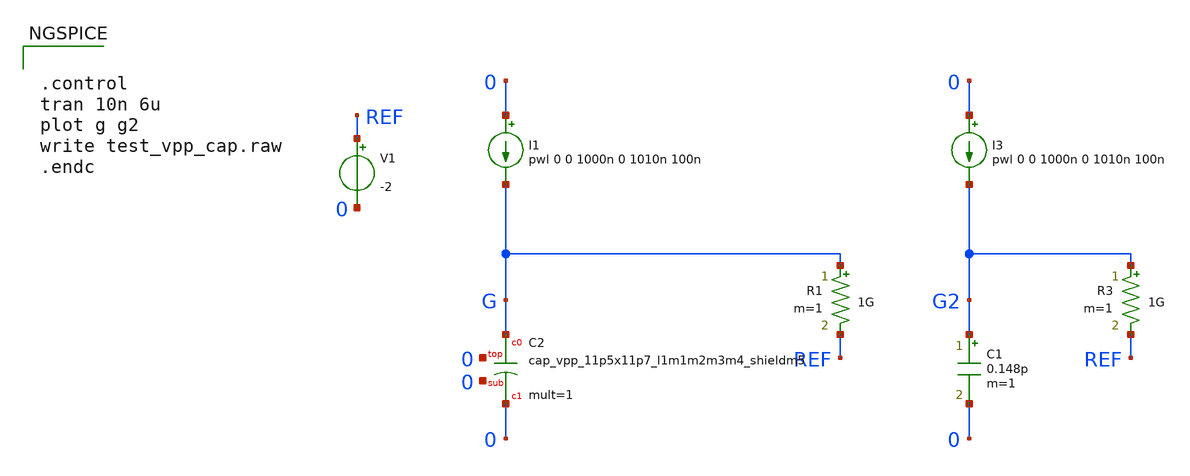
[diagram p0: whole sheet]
** sch_path: sky130_tests/test_vpp_cap.sch
* Copyright 2021 Stefan Frederik Schippers
* Licensed under the Apache License, Version 2.0 (the "License");
* you may not use this file except in compliance with the License.
* You may obtain a copy of the License at
* https://www.apache.org/licenses/LICENSE-2.0
* Unless required by applicable law or agreed to in writing, software
* distributed under the License is distributed on an "AS IS" BASIS,
* WITHOUT WARRANTIES OR CONDITIONS OF ANY KIND, either express or implied.
* See the License for the specific language governing permissions and
* limitations under the License.
**.subckt test_vpp_cap
I1 0 G pwl 0 0 1000n 0 1010n 100n
R1 G REF 1G m=1
I3 0 G2 pwl 0 0 1000n 0 1010n 100n
R3 G2 REF 1G m=1
C1 G2 0 0.148p m=1
V1 REF 0 -2
XC2 G 0 0 0 sky130_fd_pr__cap_vpp_11p5x11p7_l1m1m2m3m4_shieldm5 W=1 L=1 mult=1 m=1
**** begin user architecture code


.control
tran 10n 6u
plot g g2
write test_vpp_cap.raw
.endc


 ** manual skywater pdks install (with patches applied)
* .lib $::SKYWATER_MODELS/models/sky130.lib.spice tt

** opencircuitdesign pdks install
.lib $::SKYWATER_MODELS/sky130.lib.spice tt

.param mc_mm_switch=0
.param mc_pr_switch=0

**** end user architecture code
**.ends
.end
